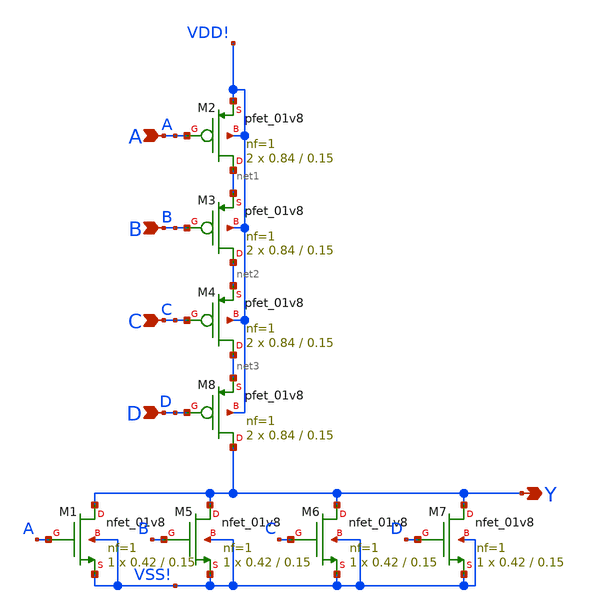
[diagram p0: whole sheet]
** sch_path: 4_nor1X/4_nor1X.sch
**.subckt 4_nor1X A B C Y D
*.ipin A
*.ipin B
*.ipin C
*.opin Y
*.ipin D
XM2 net1 A VDD! VDD! sky130_fd_pr__pfet_01v8 L=0.15 W=0.84 nf=1 ad='int((1 + 1)/2) * 0.84 / 1 * 0.29'
+ as='int((1 + 2)/2) * 0.84 / 1 * 0.29' pd='2*int((1 + 1)/2) * (0.84 / 1 + 0.29)' ps='2*int((1 + 2)/2) * (0.84 / 1 + 0.29)'
+ nrd='0.29 / 0.84 ' nrs='0.29 / 0.84 ' sa=0 sb=0 sd=0 mult=2 m=2
XM1 Y A VSS! VSS! sky130_fd_pr__nfet_01v8 L=0.15 W=0.42 nf=1 ad='int((1 + 1)/2) * 0.42 / 1 * 0.29' as='int((1 + 2)/2) * 0.42 / 1 * 0.29'
+ pd='2*int((1 + 1)/2) * (0.42 / 1 + 0.29)' ps='2*int((1 + 2)/2) * (0.42 / 1 + 0.29)' nrd='0.29 / 0.42 '
+ nrs='0.29 / 0.42 ' sa=0 sb=0 sd=0 mult=1 m=1
XM5 Y B VSS! VSS! sky130_fd_pr__nfet_01v8 L=0.15 W=0.42 nf=1 ad='int((1 + 1)/2) * 0.42 / 1 * 0.29' as='int((1 + 2)/2) * 0.42 / 1 * 0.29'
+ pd='2*int((1 + 1)/2) * (0.42 / 1 + 0.29)' ps='2*int((1 + 2)/2) * (0.42 / 1 + 0.29)' nrd='0.29 / 0.42 '
+ nrs='0.29 / 0.42 ' sa=0 sb=0 sd=0 mult=1 m=1
XM6 Y C VSS! VSS! sky130_fd_pr__nfet_01v8 L=0.15 W=0.42 nf=1 ad='int((1 + 1)/2) * 0.42 / 1 * 0.29' as='int((1 + 2)/2) * 0.42 / 1 * 0.29'
+ pd='2*int((1 + 1)/2) * (0.42 / 1 + 0.29)' ps='2*int((1 + 2)/2) * (0.42 / 1 + 0.29)' nrd='0.29 / 0.42 '
+ nrs='0.29 / 0.42 ' sa=0 sb=0 sd=0 mult=1 m=1
XM7 Y D VSS! VSS! sky130_fd_pr__nfet_01v8 L=0.15 W=0.42 nf=1 ad='int((1 + 1)/2) * 0.42 / 1 * 0.29' as='int((1 + 2)/2) * 0.42 / 1 * 0.29'
+ pd='2*int((1 + 1)/2) * (0.42 / 1 + 0.29)' ps='2*int((1 + 2)/2) * (0.42 / 1 + 0.29)' nrd='0.29 / 0.42 '
+ nrs='0.29 / 0.42 ' sa=0 sb=0 sd=0 mult=1 m=1
XM3 net2 B net1 VDD! sky130_fd_pr__pfet_01v8 L=0.15 W=0.84 nf=1 ad='int((1 + 1)/2) * 0.84 / 1 * 0.29'
+ as='int((1 + 2)/2) * 0.84 / 1 * 0.29' pd='2*int((1 + 1)/2) * (0.84 / 1 + 0.29)' ps='2*int((1 + 2)/2) * (0.84 / 1 + 0.29)'
+ nrd='0.29 / 0.84 ' nrs='0.29 / 0.84 ' sa=0 sb=0 sd=0 mult=2 m=2
XM4 net3 C net2 VDD! sky130_fd_pr__pfet_01v8 L=0.15 W=0.84 nf=1 ad='int((1 + 1)/2) * 0.84 / 1 * 0.29'
+ as='int((1 + 2)/2) * 0.84 / 1 * 0.29' pd='2*int((1 + 1)/2) * (0.84 / 1 + 0.29)' ps='2*int((1 + 2)/2) * (0.84 / 1 + 0.29)'
+ nrd='0.29 / 0.84 ' nrs='0.29 / 0.84 ' sa=0 sb=0 sd=0 mult=2 m=2
XM8 Y D net3 VDD! sky130_fd_pr__pfet_01v8 L=0.15 W=0.84 nf=1 ad='int((1 + 1)/2) * 0.84 / 1 * 0.29' as='int((1 + 2)/2) * 0.84 / 1 * 0.29'
+ pd='2*int((1 + 1)/2) * (0.84 / 1 + 0.29)' ps='2*int((1 + 2)/2) * (0.84 / 1 + 0.29)' nrd='0.29 / 0.84 '
+ nrs='0.29 / 0.84 ' sa=0 sb=0 sd=0 mult=2 m=2
**.ends
.end
